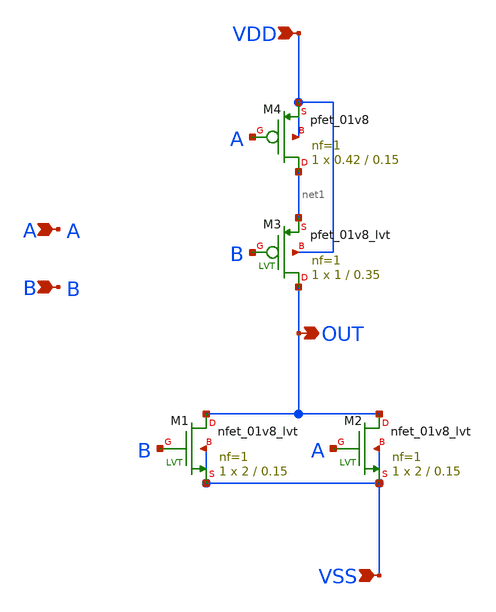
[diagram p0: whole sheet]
** sch_path: design/LELO_SVOD_SKY130A/LELO_NOR_RELOSC_DELAY.sch
**.subckt LELO_NOR_RELOSC_DELAY VDD VSS OUT A B
*.ipin VDD
*.ipin VSS
*.opin OUT
*.ipin A
*.ipin B
XM4 net1 A VDD VDD sky130_fd_pr__pfet_01v8 L=0.15 W=0.42 nf=1 ad='int((1 + 1)/2) * 0.42 / 1 * 0.29' as='int((1 + 2)/2) * 0.42 / 1 * 0.29'
+ pd='2*int((1 + 1)/2) * (0.42 / 1 + 0.29)' ps='2*int((1 + 2)/2) * (0.42 / 1 + 0.29)' nrd='0.29 / 0.42 '
+ nrs='0.29 / 0.42 ' sa=0 sb=0 sd=0 mult=1 m=1
XM3 OUT B net1 VDD sky130_fd_pr__pfet_01v8_lvt L=0.35 W=1 nf=1 ad='int((1 + 1)/2) * 1 / 1 * 0.29' as='int((1 + 2)/2) * 1 / 1 * 0.29'
+ pd='2*int((1 + 1)/2) * (1 / 1 + 0.29)' ps='2*int((1 + 2)/2) * (1 / 1 + 0.29)' nrd='0.29 / 1 ' nrs='0.29 / 1 '
+ sa=0 sb=0 sd=0 mult=1 m=1
XM1 OUT B VSS VSS sky130_fd_pr__nfet_01v8_lvt L=0.15 W=2 nf=1 ad='int((1 + 1)/2) * 2 / 1 * 0.29' as='int((1 + 2)/2) * 2 / 1 * 0.29'
+ pd='2*int((1 + 1)/2) * (2 / 1 + 0.29)' ps='2*int((1 + 2)/2) * (2 / 1 + 0.29)' nrd='0.29 / 2 ' nrs='0.29 / 2 '
+ sa=0 sb=0 sd=0 mult=1 m=1
XM2 OUT A VSS VSS sky130_fd_pr__nfet_01v8_lvt L=0.15 W=2 nf=1 ad='int((1 + 1)/2) * 2 / 1 * 0.29' as='int((1 + 2)/2) * 2 / 1 * 0.29'
+ pd='2*int((1 + 1)/2) * (2 / 1 + 0.29)' ps='2*int((1 + 2)/2) * (2 / 1 + 0.29)' nrd='0.29 / 2 ' nrs='0.29 / 2 '
+ sa=0 sb=0 sd=0 mult=1 m=1
**.ends
.end
